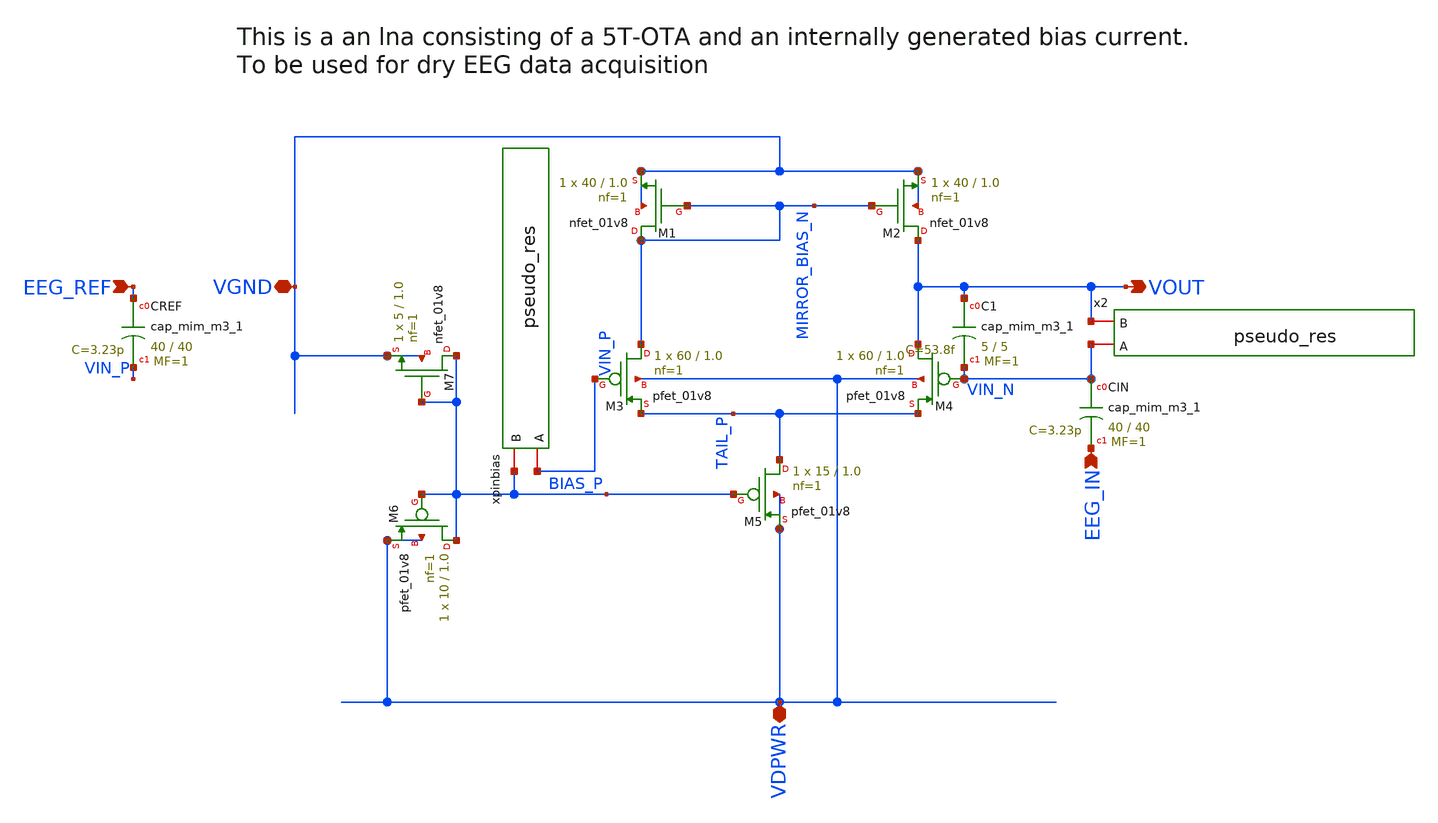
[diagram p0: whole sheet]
** sch_path: xschem/eeg_lna.sch
**.subckt eeg_lna VGND EEG_REF VDPWR VOUT EEG_IN
*.iopin VGND
*.ipin EEG_REF
*.iopin VDPWR
*.opin VOUT
*.ipin EEG_IN
XM1 MIRROR_BIAS_N MIRROR_BIAS_N VGND VGND sky130_fd_pr__nfet_01v8 L=1.0 W=40 nf=1 ad='int((1 + 1)/2) * 40 / 1 * 0.29'
+ as='int((1 + 2)/2) * 40 / 1 * 0.29' pd='2*int((1 + 1)/2) * (40 / 1 + 0.29)' ps='2*int((1 + 2)/2) * (40 / 1 + 0.29)'
+ nrd='0.29 / 40 ' nrs='0.29 / 40 ' sa=0 sb=0 sd=0 mult=1 m=1
XM2 VOUT MIRROR_BIAS_N VGND VGND sky130_fd_pr__nfet_01v8 L=1.0 W=40 nf=1 ad='int((1 + 1)/2) * 40 / 1 * 0.29'
+ as='int((1 + 2)/2) * 40 / 1 * 0.29' pd='2*int((1 + 1)/2) * (40 / 1 + 0.29)' ps='2*int((1 + 2)/2) * (40 / 1 + 0.29)'
+ nrd='0.29 / 40 ' nrs='0.29 / 40 ' sa=0 sb=0 sd=0 mult=1 m=1
XM3 MIRROR_BIAS_N VIN_P TAIL_P VDPWR sky130_fd_pr__pfet_01v8 L=1.0 W=60 nf=1 ad='int((1 + 1)/2) * 60 / 1 * 0.29'
+ as='int((1 + 2)/2) * 60 / 1 * 0.29' pd='2*int((1 + 1)/2) * (60 / 1 + 0.29)' ps='2*int((1 + 2)/2) * (60 / 1 + 0.29)'
+ nrd='0.29 / 60 ' nrs='0.29 / 60 ' sa=0 sb=0 sd=0 mult=1 m=1
XM4 VOUT VIN_N TAIL_P VDPWR sky130_fd_pr__pfet_01v8 L=1.0 W=60 nf=1 ad='int((1 + 1)/2) * 60 / 1 * 0.29'
+ as='int((1 + 2)/2) * 60 / 1 * 0.29' pd='2*int((1 + 1)/2) * (60 / 1 + 0.29)' ps='2*int((1 + 2)/2) * (60 / 1 + 0.29)'
+ nrd='0.29 / 60 ' nrs='0.29 / 60 ' sa=0 sb=0 sd=0 mult=1 m=1
XM5 TAIL_P BIAS_P VDPWR VDPWR sky130_fd_pr__pfet_01v8 L=1.0 W=15 nf=1 ad='int((1 + 1)/2) * 15 / 1 * 0.29'
+ as='int((1 + 2)/2) * 15 / 1 * 0.29' pd='2*int((1 + 1)/2) * (15 / 1 + 0.29)' ps='2*int((1 + 2)/2) * (15 / 1 + 0.29)'
+ nrd='0.29 / 15 ' nrs='0.29 / 15 ' sa=0 sb=0 sd=0 mult=1 m=1
XM6 BIAS_P BIAS_P VDPWR VDPWR sky130_fd_pr__pfet_01v8 L=1.0 W=10 nf=1 ad='int((1 + 1)/2) * 10 / 1 * 0.29'
+ as='int((1 + 2)/2) * 10 / 1 * 0.29' pd='2*int((1 + 1)/2) * (10 / 1 + 0.29)' ps='2*int((1 + 2)/2) * (10 / 1 + 0.29)'
+ nrd='0.29 / 10 ' nrs='0.29 / 10 ' sa=0 sb=0 sd=0 mult=1 m=1
XM7 BIAS_P BIAS_P VGND VGND sky130_fd_pr__nfet_01v8 L=1.0 W=5 nf=1 ad='int((1 + 1)/2) * 5 / 1 * 0.29'
+ as='int((1 + 2)/2) * 5 / 1 * 0.29' pd='2*int((1 + 1)/2) * (5 / 1 + 0.29)' ps='2*int((1 + 2)/2) * (5 / 1 + 0.29)'
+ nrd='0.29 / 5 ' nrs='0.29 / 5 ' sa=0 sb=0 sd=0 mult=1 m=1
XCIN VIN_N EEG_IN sky130_fd_pr__cap_mim_m3_1 W=40 L=40 MF=1 m=1
XCREF EEG_REF VIN_P sky130_fd_pr__cap_mim_m3_1 W=40 L=40 MF=1 m=1
xpinbias BIAS_P VIN_P pseudo_res
x2 VOUT VIN_N pseudo_res
XC1 VOUT VIN_N sky130_fd_pr__cap_mim_m3_1 W=5 L=5 MF=1 m=1
**.ends

* expanding   symbol:  pseudo_res.sym # of pins=2
** sym_path: xschem/pseudo_res.sym
** sch_path: xschem/pseudo_res.sch
.subckt pseudo_res B A
*.iopin A
*.iopin B
XM1_PSEUDO_RES B B A A sky130_fd_pr__pfet_01v8 L=10 W=0.42 nf=1 ad='int((1 + 1)/2) * 0.42 / 1 * 0.29'
+ as='int((1 + 2)/2) * 0.42 / 1 * 0.29' pd='2*int((1 + 1)/2) * (0.42 / 1 + 0.29)' ps='2*int((1 + 2)/2) * (0.42 / 1 + 0.29)'
+ nrd='0.29 / 0.42 ' nrs='0.29 / 0.42 ' sa=0 sb=0 sd=0 mult=1 m=1
XM2_PSEUDO_RES A A B B sky130_fd_pr__pfet_01v8 L=10 W=0.42 nf=1 ad='int((1 + 1)/2) * 0.42 / 1 * 0.29'
+ as='int((1 + 2)/2) * 0.42 / 1 * 0.29' pd='2*int((1 + 1)/2) * (0.42 / 1 + 0.29)' ps='2*int((1 + 2)/2) * (0.42 / 1 + 0.29)'
+ nrd='0.29 / 0.42 ' nrs='0.29 / 0.42 ' sa=0 sb=0 sd=0 mult=1 m=1
.ends

.end
